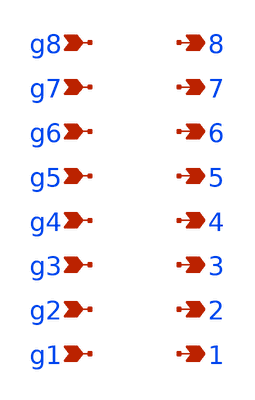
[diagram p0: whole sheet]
** sch_path: xschem/adc/8bitgray2bin.sch
**.subckt 8bitgray2bin 7 6 5 4 3 2 1 8 g5 g4 g3 g8 g7 g6 g2 g1
*.opin 7
*.opin 6
*.opin 5
*.opin 4
*.opin 3
*.opin 2
*.opin 1
*.opin 8
*.ipin g5
*.ipin g4
*.ipin g3
*.ipin g8
*.ipin g7
*.ipin g6
*.ipin g2
*.ipin g1
**** begin user architecture code


* lsb first.
a1 [g1 g2 g3 g4 g5 g6 g7 g8] [1 2 3 4 5 6 7 8] gray2bin_lut
.model gray2bin_lut d_genlut(rise_delay=[1p 1p] fall_delay=[1p 1p]  input_load=[1p 1p]
+ input_delay=[0 0]
+ table_values=01101001100101101001011001101001100101100110100101101001100101101001011001101001011010011001011001101001100101101001011001101001100101100110100101101001100101100110100110010110100101100110100101101001100101101001011001101001100101100110100101101001100101100011110011000011110000110011110011000011001111000011110011000011110000110011110000111100110000110011110011000011110000110011110011000011001111000011110011000011001111001100001111000011001111000011110011000011110000110011110011000011001111000011110011000011000011111111000011110000000011111111000000001111000011111111000011110000000011110000111111110000000011111111000011110000000011111111000000001111000011111111000000001111111100001111000000001111000011111111000011110000000011111111000000001111000011111111000000000000111111111111111100000000111111110000000000000000111111111111111100000000000000001111111100000000111111111111111100000000111111110000000000000000111111110000000011111111111111110000000000000000111111111111111100000000111111110000000000000000111111110000000000000000111111111111111111111111111111110000000000000000111111111111111100000000000000000000000000000000111111111111111111111111111111110000000000000000000000000000000011111111111111110000000000000000111111111111111111111111111111110000000000000000000000000000000000000000000000001111111111111111111111111111111111111111111111111111111111111111000000000000000000000000000000001111111111111111111111111111111100000000000000000000000000000000000000000000000000000000000000001111111111111111111111111111111100000000000000000000000000000000000000000000000000000000000000001111111111111111111111111111111111111111111111111111111111111111111111111111111111111111111111111111111111111111111111111111111100000000000000000000000000000000000000000000000000000000000000000000000000000000000000000000000000000000000000000000000000000000000000000000000000000000000000000000000000000000000000000000000011111111111111111111111111111111111111111111111111111111111111111111111111111111111111111111111111111111111111111111111111111111)




**** end user architecture code
**.ends
.end
